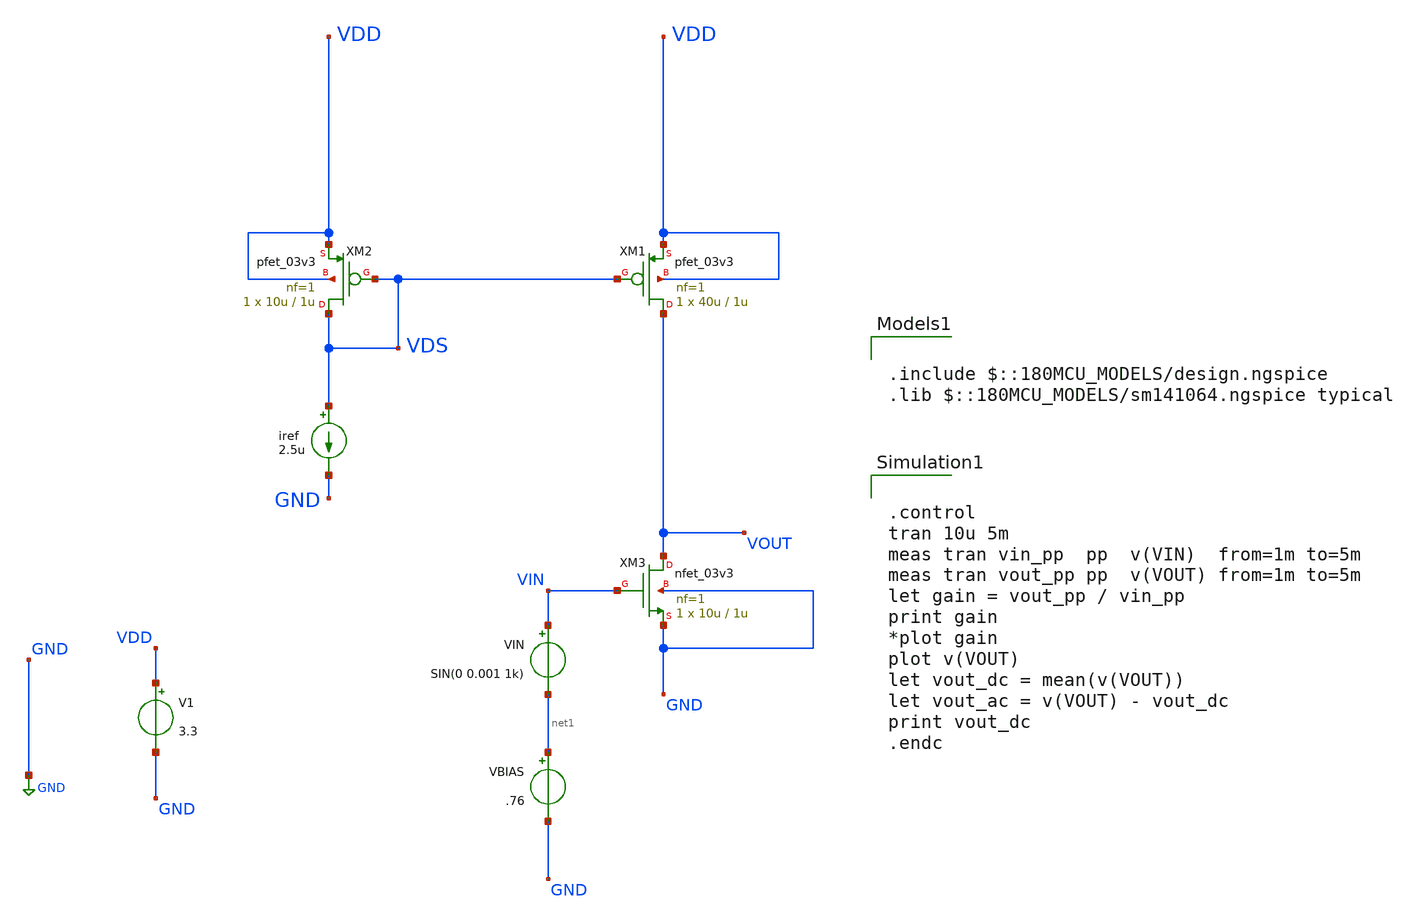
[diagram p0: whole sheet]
** sch_path: designs/libs/session_2/cs_active_load_amp.sch
**.subckt cs_active_load_amp
iref VDS GND 2.5u
XM1 VOUT VDS VDD VDD pfet_03v3 L=1u W=40u nf=1 ad='int((nf+1)/2) * W/nf * 0.18u' as='int((nf+2)/2) * W/nf * 0.18u'
+ pd='2*int((nf+1)/2) * (W/nf + 0.18u)' ps='2*int((nf+2)/2) * (W/nf + 0.18u)' nrd='0.18u / W' nrs='0.18u / W'
+ sa=0 sb=0 sd=0 m=1
XM2 VDS VDS VDD VDD pfet_03v3 L=1u W=10u nf=1 ad='int((nf+1)/2) * W/nf * 0.18u' as='int((nf+2)/2) * W/nf * 0.18u'
+ pd='2*int((nf+1)/2) * (W/nf + 0.18u)' ps='2*int((nf+2)/2) * (W/nf + 0.18u)' nrd='0.18u / W' nrs='0.18u / W'
+ sa=0 sb=0 sd=0 m=1
XM3 VOUT VIN GND GND nfet_03v3 L=1u W=10u nf=1 ad='int((nf+1)/2) * W/nf * 0.18u' as='int((nf+2)/2) * W/nf * 0.18u'
+ pd='2*int((nf+1)/2) * (W/nf + 0.18u)' ps='2*int((nf+2)/2) * (W/nf + 0.18u)' nrd='0.18u / W' nrs='0.18u / W'
+ sa=0 sb=0 sd=0 m=1
V1 VDD GND 3.3
VBIAS net1 GND .76
VIN VIN net1 SIN(0 0.001 1k)
**** begin user architecture code


.control
tran 10u 5m
meas tran vin_pp  pp  v(VIN)  from=1m to=5m
meas tran vout_pp pp  v(VOUT) from=1m to=5m
let gain = vout_pp / vin_pp
print gain
*plot gain
plot v(VOUT)
let vout_dc = mean(v(VOUT))
let vout_ac = v(VOUT) - vout_dc
print vout_dc
.endc



.include $::180MCU_MODELS/design.ngspice
.lib $::180MCU_MODELS/sm141064.ngspice typical

**** end user architecture code
**.ends
.GLOBAL GND
.end
